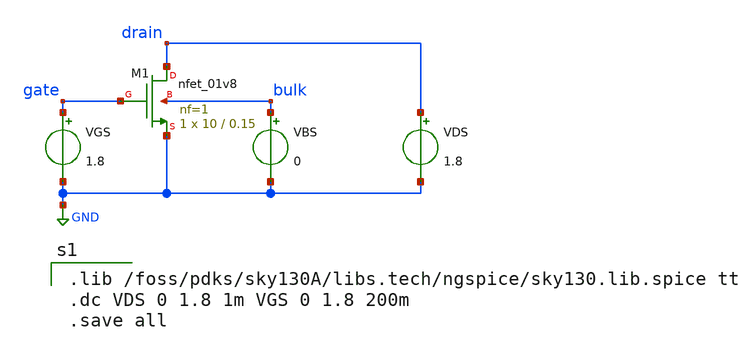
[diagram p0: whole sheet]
** sch_path: designs/reference/nmost.sch
**.subckt nmost
XM1 drain gate GND bulk sky130_fd_pr__nfet_01v8 L=0.15 W=10 nf=1 ad='int((nf+1)/2) * W/nf * 0.29' as='int((nf+2)/2) * W/nf * 0.29'
+ pd='2*int((nf+1)/2) * (W/nf + 0.29)' ps='2*int((nf+2)/2) * (W/nf + 0.29)' nrd='0.29 / W' nrs='0.29 / W'
+ sa=0 sb=0 sd=0 mult=1 m=1
VDS drain GND 1.8
VBS bulk GND 0
VGS gate GND 1.8
**** begin user architecture code

.lib /foss/pdks/sky130A/libs.tech/ngspice/sky130.lib.spice tt
.dc VDS 0 1.8 1m VGS 0 1.8 200m
.save all

**** end user architecture code
**.ends
.GLOBAL GND
.end
